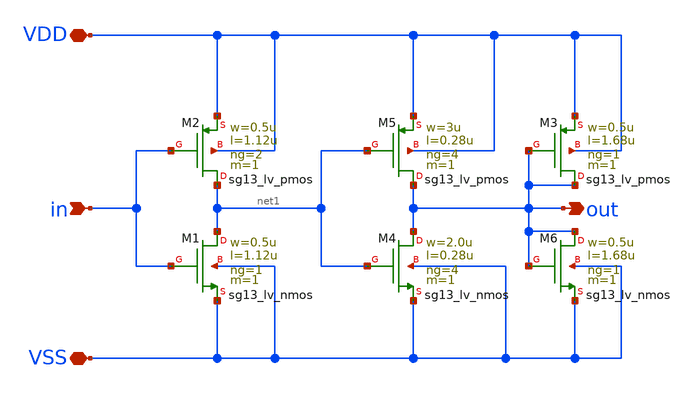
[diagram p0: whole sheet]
** sch_path: blocks/composite/dpi_adexp_neuron/design_data/xschem/dev/pex.sch
**.subckt pex VDD in VSS out
*.iopin VDD
*.ipin in
*.iopin VSS
*.opin out
XM1 net1 in VSS VSS sg13_lv_nmos w=0.5u l=1.12u ng=1 m=1 mm_ok=1
XM2 net1 in VDD VDD sg13_lv_pmos w=0.5u l=1.12u ng=2 m=1 mm_ok=1
XM4 out net1 VSS VSS sg13_lv_nmos w=2.0u l=0.28u ng=4 m=1 mm_ok=1
XM5 out net1 VDD VDD sg13_lv_pmos w=3u l=0.28u ng=4 m=1 mm_ok=1
XM3 out out VDD VDD sg13_lv_pmos w=0.5u l=1.68u ng=1 m=1 mm_ok=1
XM6 out out VSS VSS sg13_lv_nmos w=0.5u l=1.68u ng=1 m=1 mm_ok=1
**.ends
.end
